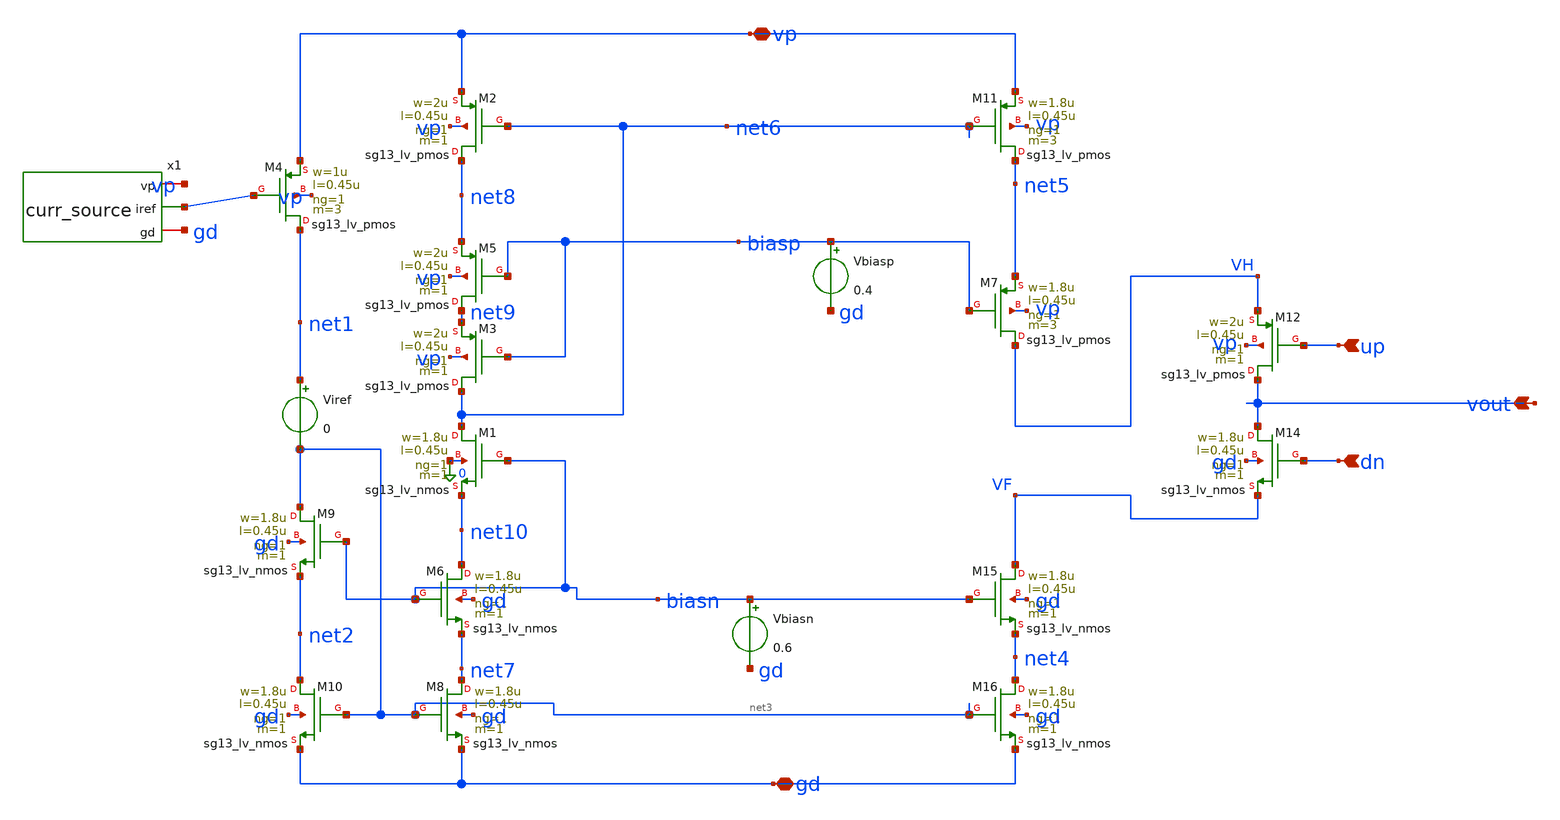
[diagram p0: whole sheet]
** sch_path: PLL0663-main/schematic/xschem/charge_pump/old_sch/cp_v1_new_low_curr.sch
**.subckt cp_v1_new_low_curr up dn vp gd vout
*.ipin up
*.ipin dn
*.iopin vp
*.iopin gd
*.opin vout
XM7 VH biasp net5 vp sg13_lv_pmos w=1.8u l=0.45u ng=1 m=3 mm_ok=1
XM12 vout up VH vp sg13_lv_pmos w=2u l=0.45u ng=1 m=1 mm_ok=1
XM14 vout dn VF gd sg13_lv_nmos w=1.8u l=0.45u ng=1 m=1 mm_ok=1
XM15 VF biasn net4 gd sg13_lv_nmos w=1.8u l=0.45u ng=1 m=1 mm_ok=1
XM16 net4 net3 gd gd sg13_lv_nmos w=1.8u l=0.45u ng=1 m=1 mm_ok=1
XM1 net6 biasn net10 0 sg13_lv_nmos w=1.8u l=0.45u ng=1 m=1 mm_ok=1
XM2 net8 net6 vp vp sg13_lv_pmos w=2u l=0.45u ng=1 m=1 mm_ok=1
XM5 net9 biasp net8 vp sg13_lv_pmos w=2u l=0.45u ng=1 m=1 mm_ok=1
XM3 net6 biasp net9 vp sg13_lv_pmos w=2u l=0.45u ng=1 m=1 mm_ok=1
XM6 net10 biasn net7 gd sg13_lv_nmos w=1.8u l=0.45u ng=1 m=1 mm_ok=1
XM8 net7 net3 gd gd sg13_lv_nmos w=1.8u l=0.45u ng=1 m=1 mm_ok=1
XM9 net3 biasn net2 gd sg13_lv_nmos w=1.8u l=0.45u ng=1 m=1 mm_ok=1
XM10 net2 net3 gd gd sg13_lv_nmos w=1.8u l=0.45u ng=1 m=1 mm_ok=1
XM11 net5 net6 vp vp sg13_lv_pmos w=1.8u l=0.45u ng=1 m=3 mm_ok=1
Vbiasp biasp gd 0.4
Vbiasn biasn gd 0.6
XM4 net1 net11 vp vp sg13_lv_pmos w=1u l=0.45u ng=1 m=3 mm_ok=1
x1 vp net11 gd curr_source
Viref net1 net3 0
**.ends

* expanding   symbol:
*+  /foss/designs/IHP__PLL0663/PLL0663-main/schematic/xschem/charge_pump/curr_source.sym # of pins=3
** sym_path: /foss/designs/IHP__PLL0663/PLL0663-main/schematic/xschem/charge_pump/curr_source.sym
** sch_path: /foss/designs/IHP__PLL0663/PLL0663-main/schematic/xschem/charge_pump/curr_source.sch
.subckt curr_source vp iref gd
*.iopin vp
*.iopin gd
*.opin iref
XM9 net3 net3 gd gd sg13_lv_nmos w=1u l=0.6u ng=1 m=1 mm_ok=1
XM4 iref iref vp vp sg13_lv_pmos w=1.4u l=0.6u ng=1 m=1 mm_ok=1
XM5 net2 iref vp vp sg13_lv_pmos w=1.2u l=0.6u ng=1 m=1 mm_ok=1
XM10 iref net2 net1 gd sg13_lv_nmos w=1.2u l=0.6u ng=1 m=1 mm_ok=1
XM1 net2 net2 gd gd sg13_lv_nmos w=1.4u l=0.6u ng=1 m=1 mm_ok=1
XM3 vp vp net3 gd sg13_lv_nmos w=1u l=0.6u ng=1 m=1 mm_ok=1
XM6 vp net3 iref gd sg13_lv_nmos w=1u l=0.6u ng=1 m=1 mm_ok=1
XM2 gd gd gd gd sg13_lv_nmos w=0.4u l=0.6u ng=1 m=1 mm_ok=1
XR2 net1 gd gd rppd w=1e-6 l=1.7e-6 m=1 b=0 mm_ok=1
.ends

.end
